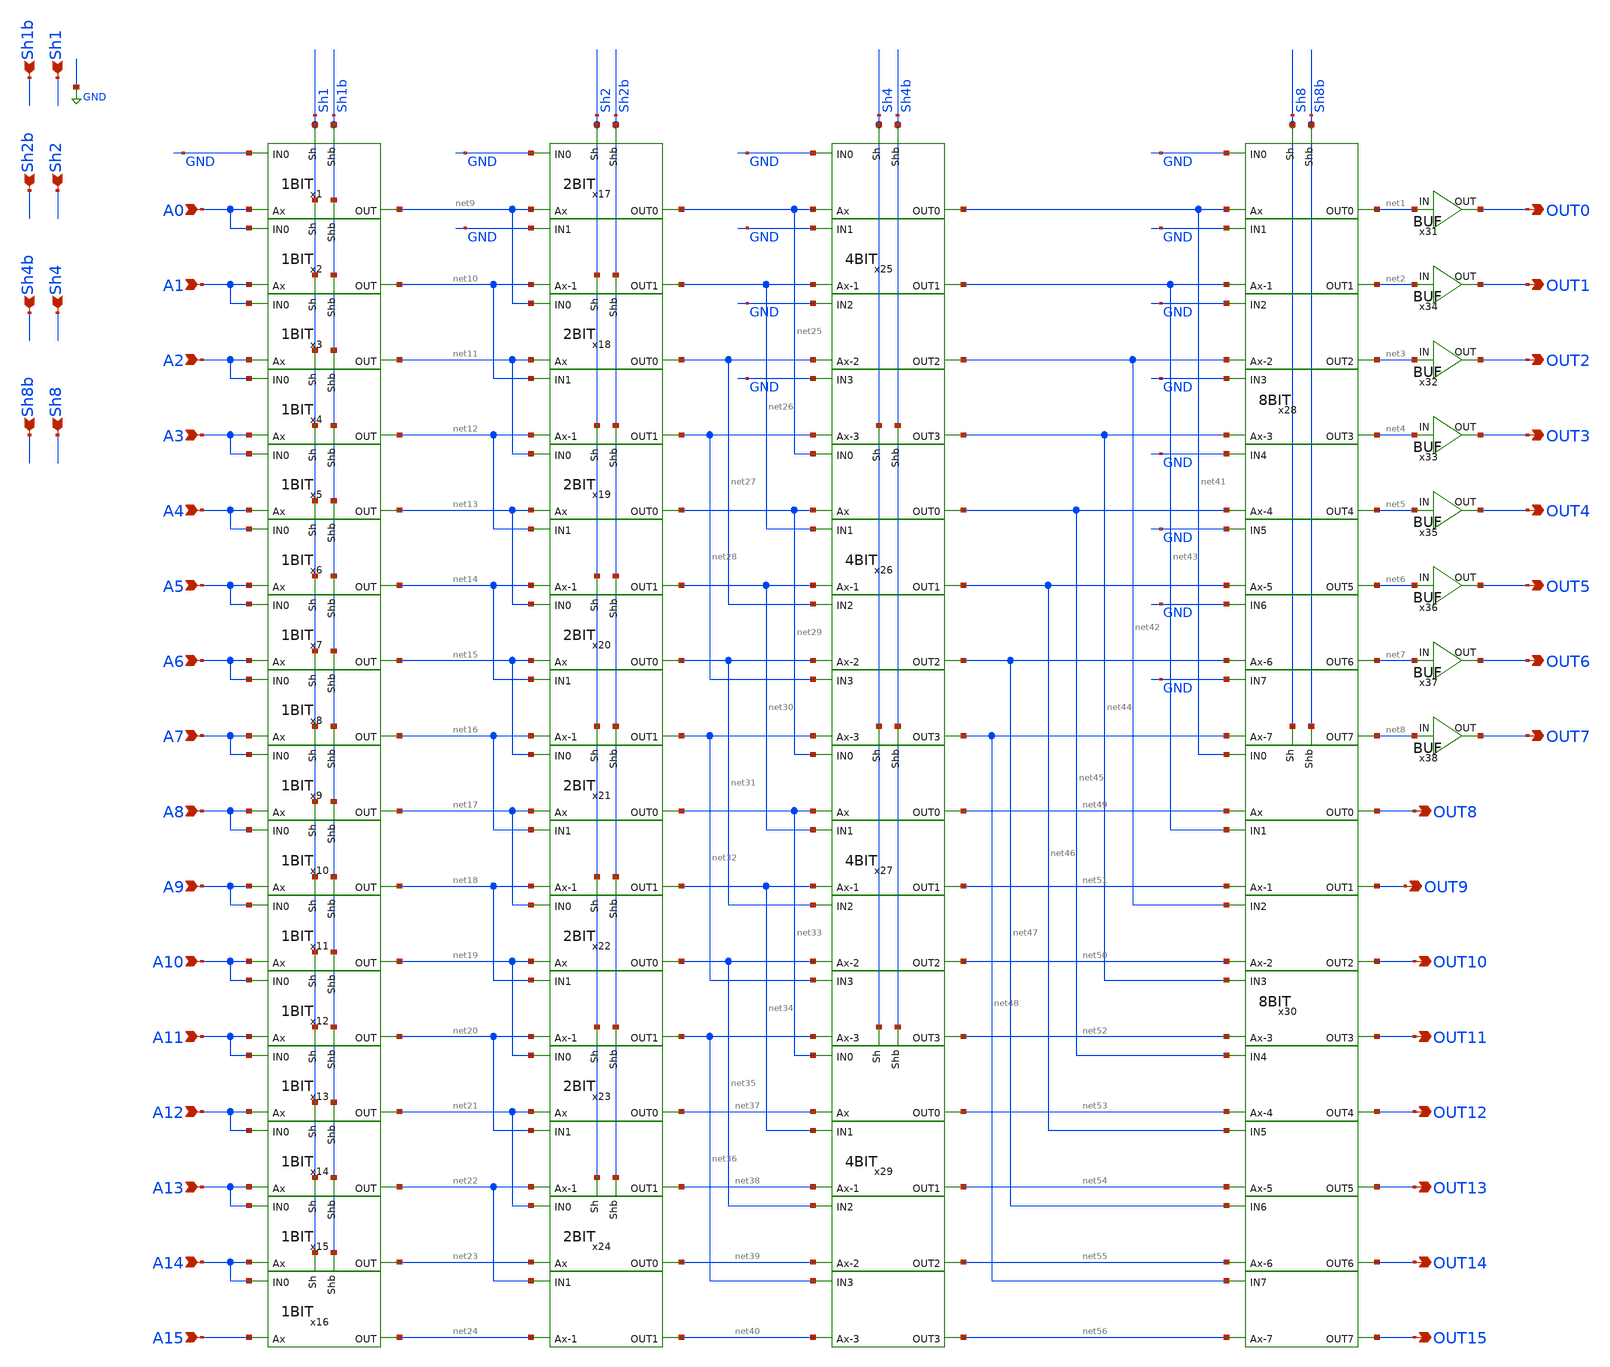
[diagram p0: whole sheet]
** sch_path: SHIFT.sch
**.subckt SHIFT Sh1 Sh1b A0 A1 A2 A3 A4 A5 A6 A7 A8 A9 A10 A11 A12 A13 A14 A15 OUT0 OUT1 OUT2 OUT3
*+ OUT4 OUT5 OUT6 OUT7 OUT8 OUT9 OUT10 OUT11 OUT12 OUT13 OUT14 OUT15 Sh2 Sh2b Sh4 Sh4b Sh8 Sh8b
*.ipin Sh1
*.ipin Sh1b
*.ipin A0
*.ipin A1
*.ipin A2
*.ipin A3
*.ipin A4
*.ipin A5
*.ipin A6
*.ipin A7
*.ipin A8
*.ipin A9
*.ipin A10
*.ipin A11
*.ipin A12
*.ipin A13
*.ipin A14
*.ipin A15
*.opin OUT0
*.opin OUT1
*.opin OUT2
*.opin OUT3
*.opin OUT4
*.opin OUT5
*.opin OUT6
*.opin OUT7
*.opin OUT8
*.opin OUT9
*.opin OUT10
*.opin OUT11
*.opin OUT12
*.opin OUT13
*.opin OUT14
*.opin OUT15
*.ipin Sh2
*.ipin Sh2b
*.ipin Sh4
*.ipin Sh4b
*.ipin Sh8
*.ipin Sh8b
x1 Sh1b Sh1 A0 GND net9 1BIT
x2 Sh1b Sh1 A1 A0 net10 1BIT
x3 Sh1b Sh1 A2 A1 net11 1BIT
x4 Sh1b Sh1 A3 A2 net12 1BIT
x5 Sh1b Sh1 A4 A3 net13 1BIT
x6 Sh1b Sh1 A5 A4 net14 1BIT
x7 Sh1b Sh1 A6 A5 net15 1BIT
x8 Sh1b Sh1 A7 A6 net16 1BIT
x9 Sh1b Sh1 A8 A7 net17 1BIT
x10 Sh1b Sh1 A9 A8 net18 1BIT
x11 Sh1b Sh1 A10 A9 net19 1BIT
x12 Sh1b Sh1 A11 A10 net20 1BIT
x13 Sh1b Sh1 A12 A11 net21 1BIT
x14 Sh1b Sh1 A13 A12 net22 1BIT
x15 Sh1b Sh1 A14 A13 net23 1BIT
x16 Sh1b Sh1 A15 A14 net24 1BIT
x17 Sh2b Sh2 net9 GND net25 net26 GND net10 2BIT
x18 Sh2b Sh2 net11 net9 net27 net28 net10 net12 2BIT
x19 Sh2b Sh2 net13 net11 net29 net30 net12 net14 2BIT
x20 Sh2b Sh2 net15 net13 net31 net32 net14 net16 2BIT
x21 Sh2b Sh2 net17 net15 net33 net34 net16 net18 2BIT
x22 Sh2b Sh2 net19 net17 net35 net36 net18 net20 2BIT
x23 Sh2b Sh2 net21 net19 net37 net38 net20 net22 2BIT
x24 Sh2b Sh2 net23 net21 net39 net40 net22 net24 2BIT
x25 Sh4b Sh4 GND net25 net41 net43 net42 net44 GND net26 GND net27 GND net28 4BIT
x26 Sh4b Sh4 net25 net29 net45 net46 net47 net48 net26 net30 net27 net31 net28 net32 4BIT
x27 Sh4b Sh4 net29 net33 net49 net51 net50 net52 net30 net34 net31 net35 net32 net36 4BIT
x29 Sh4b Sh4 net33 net37 net53 net54 net55 net56 net34 net38 net35 net39 net36 net40 4BIT
x28 Sh8b Sh8 net41 GND net1 net2 net3 net4 net43 GND GND net42 GND net44 net45 GND net5 net6 net7
+ net8 GND net46 GND net47 GND net48 8BIT
x30 Sh8b Sh8 net49 net41 OUT8 OUT9 OUT10 OUT11 net51 net43 net42 net50 net44 net52 net53 net45 OUT12
+ OUT13 OUT14 OUT15 net46 net54 net47 net55 net48 net56 8BIT
x31 OUT0 net1 BUF
x32 OUT2 net3 BUF
x33 OUT3 net4 BUF
x34 OUT1 net2 BUF
x35 OUT4 net5 BUF
x36 OUT5 net6 BUF
x37 OUT6 net7 BUF
x38 OUT7 net8 BUF
**.ends
.GLOBAL GND
.end
